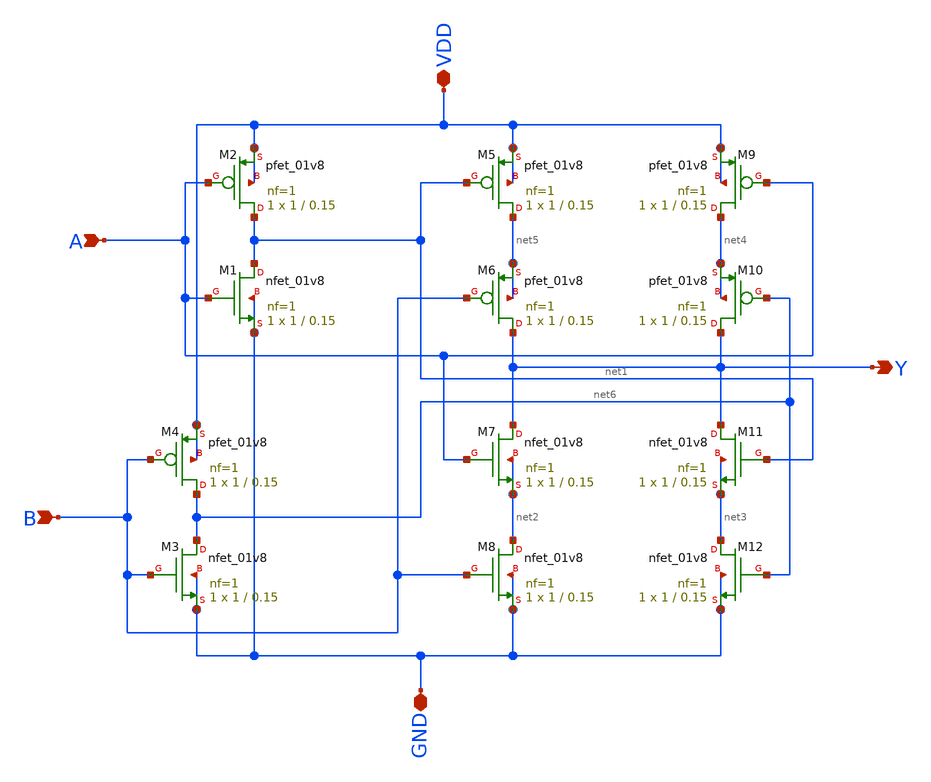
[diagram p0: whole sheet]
** sch_path: designs/xor12t/xschem/xor.sch
**.subckt xor A B Y GND VDD
*.ipin A
*.ipin B
*.opin Y
*.iopin GND
*.iopin VDD
XM1 net1 A GND GND sky130_fd_pr__nfet_01v8 L=0.15 W=1 nf=1 ad='int((1 + 1)/2) * 1 / 1 * 0.29' as='int((1 + 2)/2) * 1 / 1 * 0.29'
+ pd='2*int((1 + 1)/2) * (1 / 1 + 0.29)' ps='2*int((1 + 2)/2) * (1 / 1 + 0.29)' nrd='0.29 / 1 ' nrs='0.29 / 1 '
+ sa=0 sb=0 sd=0 mult=1 m=1
XM2 net1 A VDD VDD sky130_fd_pr__pfet_01v8 L=0.15 W=1 nf=1 ad='int((1 + 1)/2) * 1 / 1 * 0.29' as='int((1 + 2)/2) * 1 / 1 * 0.29'
+ pd='2*int((1 + 1)/2) * (1 / 1 + 0.29)' ps='2*int((1 + 2)/2) * (1 / 1 + 0.29)' nrd='0.29 / 1 ' nrs='0.29 / 1 '
+ sa=0 sb=0 sd=0 mult=1 m=1
XM3 net6 B GND GND sky130_fd_pr__nfet_01v8 L=0.15 W=1 nf=1 ad='int((1 + 1)/2) * 1 / 1 * 0.29' as='int((1 + 2)/2) * 1 / 1 * 0.29'
+ pd='2*int((1 + 1)/2) * (1 / 1 + 0.29)' ps='2*int((1 + 2)/2) * (1 / 1 + 0.29)' nrd='0.29 / 1 ' nrs='0.29 / 1 '
+ sa=0 sb=0 sd=0 mult=1 m=1
XM4 net6 B VDD VDD sky130_fd_pr__pfet_01v8 L=0.15 W=1 nf=1 ad='int((1 + 1)/2) * 1 / 1 * 0.29' as='int((1 + 2)/2) * 1 / 1 * 0.29'
+ pd='2*int((1 + 1)/2) * (1 / 1 + 0.29)' ps='2*int((1 + 2)/2) * (1 / 1 + 0.29)' nrd='0.29 / 1 ' nrs='0.29 / 1 '
+ sa=0 sb=0 sd=0 mult=1 m=1
XM5 net5 net1 VDD VDD sky130_fd_pr__pfet_01v8 L=0.15 W=1 nf=1 ad='int((1 + 1)/2) * 1 / 1 * 0.29' as='int((1 + 2)/2) * 1 / 1 * 0.29'
+ pd='2*int((1 + 1)/2) * (1 / 1 + 0.29)' ps='2*int((1 + 2)/2) * (1 / 1 + 0.29)' nrd='0.29 / 1 ' nrs='0.29 / 1 '
+ sa=0 sb=0 sd=0 mult=1 m=1
XM6 Y B net5 net5 sky130_fd_pr__pfet_01v8 L=0.15 W=1 nf=1 ad='int((1 + 1)/2) * 1 / 1 * 0.29' as='int((1 + 2)/2) * 1 / 1 * 0.29'
+ pd='2*int((1 + 1)/2) * (1 / 1 + 0.29)' ps='2*int((1 + 2)/2) * (1 / 1 + 0.29)' nrd='0.29 / 1 ' nrs='0.29 / 1 '
+ sa=0 sb=0 sd=0 mult=1 m=1
XM7 Y A net2 net2 sky130_fd_pr__nfet_01v8 L=0.15 W=1 nf=1 ad='int((1 + 1)/2) * 1 / 1 * 0.29' as='int((1 + 2)/2) * 1 / 1 * 0.29'
+ pd='2*int((1 + 1)/2) * (1 / 1 + 0.29)' ps='2*int((1 + 2)/2) * (1 / 1 + 0.29)' nrd='0.29 / 1 ' nrs='0.29 / 1 '
+ sa=0 sb=0 sd=0 mult=1 m=1
XM8 net2 B GND GND sky130_fd_pr__nfet_01v8 L=0.15 W=1 nf=1 ad='int((1 + 1)/2) * 1 / 1 * 0.29' as='int((1 + 2)/2) * 1 / 1 * 0.29'
+ pd='2*int((1 + 1)/2) * (1 / 1 + 0.29)' ps='2*int((1 + 2)/2) * (1 / 1 + 0.29)' nrd='0.29 / 1 ' nrs='0.29 / 1 '
+ sa=0 sb=0 sd=0 mult=1 m=1
XM9 net4 A VDD VDD sky130_fd_pr__pfet_01v8 L=0.15 W=1 nf=1 ad='int((1 + 1)/2) * 1 / 1 * 0.29' as='int((1 + 2)/2) * 1 / 1 * 0.29'
+ pd='2*int((1 + 1)/2) * (1 / 1 + 0.29)' ps='2*int((1 + 2)/2) * (1 / 1 + 0.29)' nrd='0.29 / 1 ' nrs='0.29 / 1 '
+ sa=0 sb=0 sd=0 mult=1 m=1
XM10 Y net6 net4 net4 sky130_fd_pr__pfet_01v8 L=0.15 W=1 nf=1 ad='int((1 + 1)/2) * 1 / 1 * 0.29' as='int((1 + 2)/2) * 1 / 1 * 0.29'
+ pd='2*int((1 + 1)/2) * (1 / 1 + 0.29)' ps='2*int((1 + 2)/2) * (1 / 1 + 0.29)' nrd='0.29 / 1 ' nrs='0.29 / 1 '
+ sa=0 sb=0 sd=0 mult=1 m=1
XM11 Y net1 net3 net3 sky130_fd_pr__nfet_01v8 L=0.15 W=1 nf=1 ad='int((1 + 1)/2) * 1 / 1 * 0.29' as='int((1 + 2)/2) * 1 / 1 * 0.29'
+ pd='2*int((1 + 1)/2) * (1 / 1 + 0.29)' ps='2*int((1 + 2)/2) * (1 / 1 + 0.29)' nrd='0.29 / 1 ' nrs='0.29 / 1 '
+ sa=0 sb=0 sd=0 mult=1 m=1
XM12 net3 net6 GND GND sky130_fd_pr__nfet_01v8 L=0.15 W=1 nf=1 ad='int((1 + 1)/2) * 1 / 1 * 0.29' as='int((1 + 2)/2) * 1 / 1 * 0.29'
+ pd='2*int((1 + 1)/2) * (1 / 1 + 0.29)' ps='2*int((1 + 2)/2) * (1 / 1 + 0.29)' nrd='0.29 / 1 ' nrs='0.29 / 1 '
+ sa=0 sb=0 sd=0 mult=1 m=1
**.ends
.end
